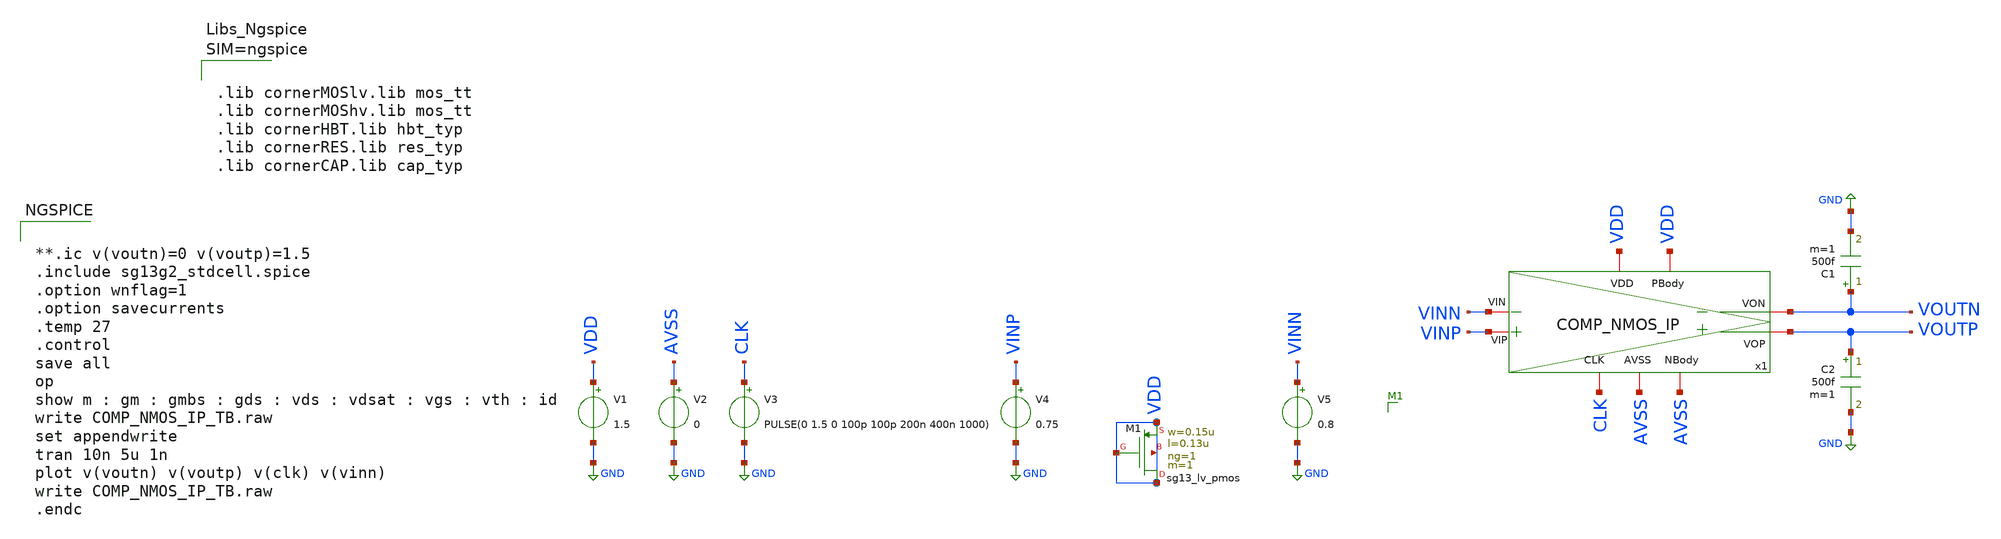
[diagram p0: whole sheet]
** sch_path: COMP/COMP_NMOS_IP_TB.sch
**.subckt COMP_NMOS_IP_TB
x1 VDD CLK VDD VOUTN VOUTP VINP VINN AVSS AVSS COMP_NMOS_IP
V1 VDD GND 1.5
V2 AVSS GND 0
V3 CLK GND PULSE(0 1.5 0 100p 100p 200n 400n 1000)
V4 VINP GND 0.75
V5 VINN GND 0.8
C1 VOUTN GND 500f m=1
C2 VOUTP GND 500f m=1
XM1 VDD VDD VDD VDD sg13_lv_pmos w=0.15u l=0.13u ng=1 m=1 mm_ok=1
**** begin user architecture code


**.ic v(voutn)=0 v(voutp)=1.5
.include sg13g2_stdcell.spice
.option wnflag=1
.option savecurrents
.temp 27
.control
save all
op
show m : gm : gmbs : gds : vds : vdsat : vgs : vth : id
write COMP_NMOS_IP_TB.raw
set appendwrite
tran 10n 5u 1n
plot v(voutn) v(voutp) v(clk) v(vinn)
write COMP_NMOS_IP_TB.raw
.endc





.lib cornerMOSlv.lib mos_tt
.lib cornerMOShv.lib mos_tt
.lib cornerHBT.lib hbt_typ
.lib cornerRES.lib res_typ
.lib cornerCAP.lib cap_typ





.save @n.x1.xmn_vip.nsg13_lv_nmos[ids]
.save @n.x1.xmn_vip.nsg13_lv_nmos[gm]
.save @n.x1.xmn_vip.nsg13_lv_nmos[gds]
.save @n.x1.xmn_vip.nsg13_lv_nmos[vth]
.save @n.x1.xmn_vip.nsg13_lv_nmos[vgs]
.save @n.x1.xmn_vip.nsg13_lv_nmos[vdss]
.save @n.x1.xmn_vip.nsg13_lv_nmos[vds]
.save @n.x1.xmn_vip.nsg13_lv_nmos[cgg]
.save @n.x1.xmn_vip.nsg13_lv_nmos[cgsol]
.save @n.x1.xmn_vip.nsg13_lv_nmos[cgdol]
.save @n.x1.xmn_vin.nsg13_lv_nmos[ids]
.save @n.x1.xmn_vin.nsg13_lv_nmos[gm]
.save @n.x1.xmn_vin.nsg13_lv_nmos[gds]
.save @n.x1.xmn_vin.nsg13_lv_nmos[vth]
.save @n.x1.xmn_vin.nsg13_lv_nmos[vgs]
.save @n.x1.xmn_vin.nsg13_lv_nmos[vdss]
.save @n.x1.xmn_vin.nsg13_lv_nmos[vds]
.save @n.x1.xmn_vin.nsg13_lv_nmos[cgg]
.save @n.x1.xmn_vin.nsg13_lv_nmos[cgsol]
.save @n.x1.xmn_vin.nsg13_lv_nmos[cgdol]
.save @n.x1.xmp_crs_cp2.nsg13_lv_pmos[ids]
.save @n.x1.xmp_crs_cp2.nsg13_lv_pmos[gm]
.save @n.x1.xmp_crs_cp2.nsg13_lv_pmos[gds]
.save @n.x1.xmp_crs_cp2.nsg13_lv_pmos[vth]
.save @n.x1.xmp_crs_cp2.nsg13_lv_pmos[vgs]
.save @n.x1.xmp_crs_cp2.nsg13_lv_pmos[vdss]
.save @n.x1.xmp_crs_cp2.nsg13_lv_pmos[vds]
.save @n.x1.xmp_crs_cp2.nsg13_lv_pmos[cgg]
.save @n.x1.xmp_crs_cp2.nsg13_lv_pmos[cgsol]
.save @n.x1.xmp_crs_cp2.nsg13_lv_pmos[cgdol]
.save @n.x1.xmp_crs_cp1.nsg13_lv_pmos[ids]
.save @n.x1.xmp_crs_cp1.nsg13_lv_pmos[gm]
.save @n.x1.xmp_crs_cp1.nsg13_lv_pmos[gds]
.save @n.x1.xmp_crs_cp1.nsg13_lv_pmos[vth]
.save @n.x1.xmp_crs_cp1.nsg13_lv_pmos[vgs]
.save @n.x1.xmp_crs_cp1.nsg13_lv_pmos[vdss]
.save @n.x1.xmp_crs_cp1.nsg13_lv_pmos[vds]
.save @n.x1.xmp_crs_cp1.nsg13_lv_pmos[cgg]
.save @n.x1.xmp_crs_cp1.nsg13_lv_pmos[cgsol]
.save @n.x1.xmp_crs_cp1.nsg13_lv_pmos[cgdol]
.save @n.x1.xmn_crs_cp1.nsg13_lv_nmos[ids]
.save @n.x1.xmn_crs_cp1.nsg13_lv_nmos[gm]
.save @n.x1.xmn_crs_cp1.nsg13_lv_nmos[gds]
.save @n.x1.xmn_crs_cp1.nsg13_lv_nmos[vth]
.save @n.x1.xmn_crs_cp1.nsg13_lv_nmos[vgs]
.save @n.x1.xmn_crs_cp1.nsg13_lv_nmos[vdss]
.save @n.x1.xmn_crs_cp1.nsg13_lv_nmos[vds]
.save @n.x1.xmn_crs_cp1.nsg13_lv_nmos[cgg]
.save @n.x1.xmn_crs_cp1.nsg13_lv_nmos[cgsol]
.save @n.x1.xmn_crs_cp1.nsg13_lv_nmos[cgdol]
.save @n.x1.xmn_crs_cp2.nsg13_lv_nmos[ids]
.save @n.x1.xmn_crs_cp2.nsg13_lv_nmos[gm]
.save @n.x1.xmn_crs_cp2.nsg13_lv_nmos[gds]
.save @n.x1.xmn_crs_cp2.nsg13_lv_nmos[vth]
.save @n.x1.xmn_crs_cp2.nsg13_lv_nmos[vgs]
.save @n.x1.xmn_crs_cp2.nsg13_lv_nmos[vdss]
.save @n.x1.xmn_crs_cp2.nsg13_lv_nmos[vds]
.save @n.x1.xmn_crs_cp2.nsg13_lv_nmos[cgg]
.save @n.x1.xmn_crs_cp2.nsg13_lv_nmos[cgsol]
.save @n.x1.xmn_crs_cp2.nsg13_lv_nmos[cgdol]
.save @n.x1.xmp_pc_out_p.nsg13_lv_pmos[ids]
.save @n.x1.xmp_pc_out_p.nsg13_lv_pmos[gm]
.save @n.x1.xmp_pc_out_p.nsg13_lv_pmos[gds]
.save @n.x1.xmp_pc_out_p.nsg13_lv_pmos[vth]
.save @n.x1.xmp_pc_out_p.nsg13_lv_pmos[vgs]
.save @n.x1.xmp_pc_out_p.nsg13_lv_pmos[vdss]
.save @n.x1.xmp_pc_out_p.nsg13_lv_pmos[vds]
.save @n.x1.xmp_pc_out_p.nsg13_lv_pmos[cgg]
.save @n.x1.xmp_pc_out_p.nsg13_lv_pmos[cgsol]
.save @n.x1.xmp_pc_out_p.nsg13_lv_pmos[cgdol]
.save @n.x1.xmp_pc_ip_p.nsg13_lv_pmos[ids]
.save @n.x1.xmp_pc_ip_p.nsg13_lv_pmos[gm]
.save @n.x1.xmp_pc_ip_p.nsg13_lv_pmos[gds]
.save @n.x1.xmp_pc_ip_p.nsg13_lv_pmos[vth]
.save @n.x1.xmp_pc_ip_p.nsg13_lv_pmos[vgs]
.save @n.x1.xmp_pc_ip_p.nsg13_lv_pmos[vdss]
.save @n.x1.xmp_pc_ip_p.nsg13_lv_pmos[vds]
.save @n.x1.xmp_pc_ip_p.nsg13_lv_pmos[cgg]
.save @n.x1.xmp_pc_ip_p.nsg13_lv_pmos[cgsol]
.save @n.x1.xmp_pc_ip_p.nsg13_lv_pmos[cgdol]
.save @n.x1.xmp_pc_out_n.nsg13_lv_pmos[ids]
.save @n.x1.xmp_pc_out_n.nsg13_lv_pmos[gm]
.save @n.x1.xmp_pc_out_n.nsg13_lv_pmos[gds]
.save @n.x1.xmp_pc_out_n.nsg13_lv_pmos[vth]
.save @n.x1.xmp_pc_out_n.nsg13_lv_pmos[vgs]
.save @n.x1.xmp_pc_out_n.nsg13_lv_pmos[vdss]
.save @n.x1.xmp_pc_out_n.nsg13_lv_pmos[vds]
.save @n.x1.xmp_pc_out_n.nsg13_lv_pmos[cgg]
.save @n.x1.xmp_pc_out_n.nsg13_lv_pmos[cgsol]
.save @n.x1.xmp_pc_out_n.nsg13_lv_pmos[cgdol]
.save @n.x1.xmp_pc_ip_n.nsg13_lv_pmos[ids]
.save @n.x1.xmp_pc_ip_n.nsg13_lv_pmos[gm]
.save @n.x1.xmp_pc_ip_n.nsg13_lv_pmos[gds]
.save @n.x1.xmp_pc_ip_n.nsg13_lv_pmos[vth]
.save @n.x1.xmp_pc_ip_n.nsg13_lv_pmos[vgs]
.save @n.x1.xmp_pc_ip_n.nsg13_lv_pmos[vdss]
.save @n.x1.xmp_pc_ip_n.nsg13_lv_pmos[vds]
.save @n.x1.xmp_pc_ip_n.nsg13_lv_pmos[cgg]
.save @n.x1.xmp_pc_ip_n.nsg13_lv_pmos[cgsol]
.save @n.x1.xmp_pc_ip_n.nsg13_lv_pmos[cgdol]
.save @n.x1.xmn_bias.nsg13_lv_nmos[ids]
.save @n.x1.xmn_bias.nsg13_lv_nmos[gm]
.save @n.x1.xmn_bias.nsg13_lv_nmos[gds]
.save @n.x1.xmn_bias.nsg13_lv_nmos[vth]
.save @n.x1.xmn_bias.nsg13_lv_nmos[vgs]
.save @n.x1.xmn_bias.nsg13_lv_nmos[vdss]
.save @n.x1.xmn_bias.nsg13_lv_nmos[vds]
.save @n.x1.xmn_bias.nsg13_lv_nmos[cgg]
.save @n.x1.xmn_bias.nsg13_lv_nmos[cgsol]
.save @n.x1.xmn_bias.nsg13_lv_nmos[cgdol]
.save @n.x1.xm1.nsg13_lv_nmos[ids]
.save @n.x1.xm1.nsg13_lv_nmos[gm]
.save @n.x1.xm1.nsg13_lv_nmos[gds]
.save @n.x1.xm1.nsg13_lv_nmos[vth]
.save @n.x1.xm1.nsg13_lv_nmos[vgs]
.save @n.x1.xm1.nsg13_lv_nmos[vdss]
.save @n.x1.xm1.nsg13_lv_nmos[vds]
.save @n.x1.xm1.nsg13_lv_nmos[cgg]
.save @n.x1.xm1.nsg13_lv_nmos[cgsol]
.save @n.x1.xm1.nsg13_lv_nmos[cgdol]
.save @n.x1.xm3.nsg13_lv_pmos[ids]
.save @n.x1.xm3.nsg13_lv_pmos[gm]
.save @n.x1.xm3.nsg13_lv_pmos[gds]
.save @n.x1.xm3.nsg13_lv_pmos[vth]
.save @n.x1.xm3.nsg13_lv_pmos[vgs]
.save @n.x1.xm3.nsg13_lv_pmos[vdss]
.save @n.x1.xm3.nsg13_lv_pmos[vds]
.save @n.x1.xm3.nsg13_lv_pmos[cgg]
.save @n.x1.xm3.nsg13_lv_pmos[cgsol]
.save @n.x1.xm3.nsg13_lv_pmos[cgdol]
.save @n.x1.xm2.nsg13_lv_nmos[ids]
.save @n.x1.xm2.nsg13_lv_nmos[gm]
.save @n.x1.xm2.nsg13_lv_nmos[gds]
.save @n.x1.xm2.nsg13_lv_nmos[vth]
.save @n.x1.xm2.nsg13_lv_nmos[vgs]
.save @n.x1.xm2.nsg13_lv_nmos[vdss]
.save @n.x1.xm2.nsg13_lv_nmos[vds]
.save @n.x1.xm2.nsg13_lv_nmos[cgg]
.save @n.x1.xm2.nsg13_lv_nmos[cgsol]
.save @n.x1.xm2.nsg13_lv_nmos[cgdol]
.save @n.x1.xm4.nsg13_lv_pmos[ids]
.save @n.x1.xm4.nsg13_lv_pmos[gm]
.save @n.x1.xm4.nsg13_lv_pmos[gds]
.save @n.x1.xm4.nsg13_lv_pmos[vth]
.save @n.x1.xm4.nsg13_lv_pmos[vgs]
.save @n.x1.xm4.nsg13_lv_pmos[vdss]
.save @n.x1.xm4.nsg13_lv_pmos[vds]
.save @n.x1.xm4.nsg13_lv_pmos[cgg]
.save @n.x1.xm4.nsg13_lv_pmos[cgsol]
.save @n.x1.xm4.nsg13_lv_pmos[cgdol]
.save @n.xm1.nsg13_lv_pmos[ids]
.save @n.xm1.nsg13_lv_pmos[gm]
.save @n.xm1.nsg13_lv_pmos[gds]
.save @n.xm1.nsg13_lv_pmos[vth]
.save @n.xm1.nsg13_lv_pmos[vgs]
.save @n.xm1.nsg13_lv_pmos[vdss]
.save @n.xm1.nsg13_lv_pmos[vds]
.save @n.xm1.nsg13_lv_pmos[cgg]
.save @n.xm1.nsg13_lv_pmos[cgsol]
.save @n.xm1.nsg13_lv_pmos[cgdol]


**** end user architecture code
**.ends

* expanding   symbol:  /foss/designs/SAR_ADC_8_Bit_IHP130/COMP/COMP_NMOS_IP.sym # of pins=9
** sym_path: COMP/COMP_NMOS_IP.sym
** sch_path: COMP/COMP_NMOS_IP.sch
.subckt COMP_NMOS_IP VDD CLK PBody VON VOP VIP VIN NBody AVSS
*.iopin VDD
*.iopin CLK
*.iopin PBody
*.iopin VON
*.iopin VOP
*.iopin VIP
*.iopin VIN
*.iopin NBody
*.iopin AVSS
XMN_VIP net5 VIP net3 NBody sg13_lv_nmos w=1u l=0.13u ng=1 m=8 mm_ok=1
XMN_VIN net4 VIN net3 NBody sg13_lv_nmos w=1u l=0.13u ng=1 m=8 mm_ok=1
XMP_CRS_CP2 net1 net2 VDD PBody sg13_lv_pmos w=0.15u l=0.13u ng=1 m=1 mm_ok=1
XMP_CRS_CP1 net2 net1 VDD PBody sg13_lv_pmos w=0.15u l=0.13u ng=1 m=1 mm_ok=1
XMN_CRS_CP1 net2 net1 net5 NBody sg13_lv_nmos w=0.15u l=0.13u ng=1 m=1 mm_ok=1
XMN_CRS_CP2 net1 net2 net4 NBody sg13_lv_nmos w=0.15u l=0.13u ng=1 m=1 mm_ok=1
XMP_PC_OUT_P net1 CLK VDD PBody sg13_lv_pmos w=0.15u l=0.13u ng=1 m=1 mm_ok=1
XMP_PC_IP_P net4 CLK VDD PBody sg13_lv_pmos w=0.15u l=0.13u ng=1 m=1 mm_ok=1
XMP_PC_OUT_N net2 CLK VDD PBody sg13_lv_pmos w=0.15u l=0.13u ng=1 m=1 mm_ok=1
XMP_PC_IP_N net5 CLK VDD PBody sg13_lv_pmos w=0.15u l=0.13u ng=1 m=1 mm_ok=1
XMN_BIAS net3 CLK AVSS NBody sg13_lv_nmos w=1u l=0.13u ng=1 m=1 mm_ok=1
.save v(net1)
.save v(net2)
.save v(net4)
.save v(net3)
.save v(vin)
.save v(vip)
.save v(clk)
XM1 VOP net2 AVSS NBody sg13_lv_nmos w=0.15u l=0.13u ng=1 m=1 mm_ok=1
XM3 VOP net2 VDD PBody sg13_lv_pmos w=1u l=0.13u ng=1 m=1 mm_ok=1
XM2 VON net1 AVSS NBody sg13_lv_nmos w=0.15u l=0.13u ng=1 m=1 mm_ok=1
XM4 VON net1 VDD PBody sg13_lv_pmos w=1u l=0.13u ng=1 m=1 mm_ok=1
.save v(net5)
.save v(clk)
.ends

.GLOBAL GND
.end
